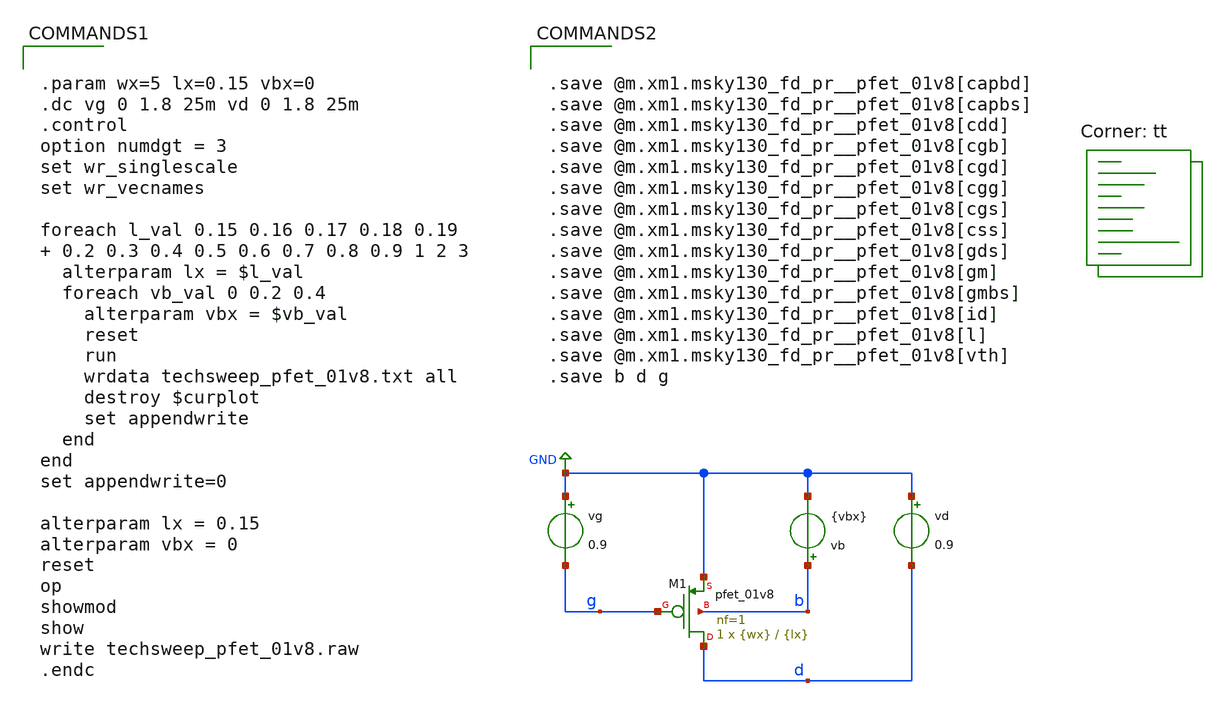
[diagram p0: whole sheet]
** sch_path: techsweep_pfet_01v8.sch
**.subckt techsweep_pfet_01v8
vg GND g 0.9
vd GND d 0.9
vb b GND {vbx}
XM1 d g GND b sky130_fd_pr__pfet_01v8 L={lx} W={wx} nf=1 ad='int((nf+1)/2) * W/nf * 0.29' as='int((nf+2)/2) * W/nf * 0.29'
+ pd='2*int((nf+1)/2) * (W/nf + 0.29)' ps='2*int((nf+2)/2) * (W/nf + 0.29)' nrd='0.29 / W' nrs='0.29 / W'
+ sa=0 sb=0 sd=0 mult=1 m=1
**** begin user architecture code


.param wx=5 lx=0.15 vbx=0
.dc vg 0 1.8 25m vd 0 1.8 25m
.control
option numdgt = 3
set wr_singlescale
set wr_vecnames

foreach l_val 0.15 0.16 0.17 0.18 0.19  0.2 0.3 0.4 0.5 0.6 0.7 0.8 0.9 1 2 3
  alterparam lx = $l_val
  foreach vb_val 0 0.2 0.4
    alterparam vbx = $vb_val
    reset
    run
    wrdata techsweep_pfet_01v8.txt all
    destroy $curplot
    set appendwrite
  end
end
set appendwrite=0

alterparam lx = 0.15
alterparam vbx = 0
reset
op
showmod
show
write techsweep_pfet_01v8.raw
.endc


.lib $::SKYWATER_MODELS/sky130.lib.spice tt


.save @m.xm1.msky130_fd_pr__pfet_01v8[capbd]
.save @m.xm1.msky130_fd_pr__pfet_01v8[capbs]
.save @m.xm1.msky130_fd_pr__pfet_01v8[cdd]
.save @m.xm1.msky130_fd_pr__pfet_01v8[cgb]
.save @m.xm1.msky130_fd_pr__pfet_01v8[cgd]
.save @m.xm1.msky130_fd_pr__pfet_01v8[cgg]
.save @m.xm1.msky130_fd_pr__pfet_01v8[cgs]
.save @m.xm1.msky130_fd_pr__pfet_01v8[css]
.save @m.xm1.msky130_fd_pr__pfet_01v8[gds]
.save @m.xm1.msky130_fd_pr__pfet_01v8[gm]
.save @m.xm1.msky130_fd_pr__pfet_01v8[gmbs]
.save @m.xm1.msky130_fd_pr__pfet_01v8[id]
.save @m.xm1.msky130_fd_pr__pfet_01v8[l]
.save @m.xm1.msky130_fd_pr__pfet_01v8[vth]
.save b d g


**** end user architecture code
**.ends
.GLOBAL GND
.end
